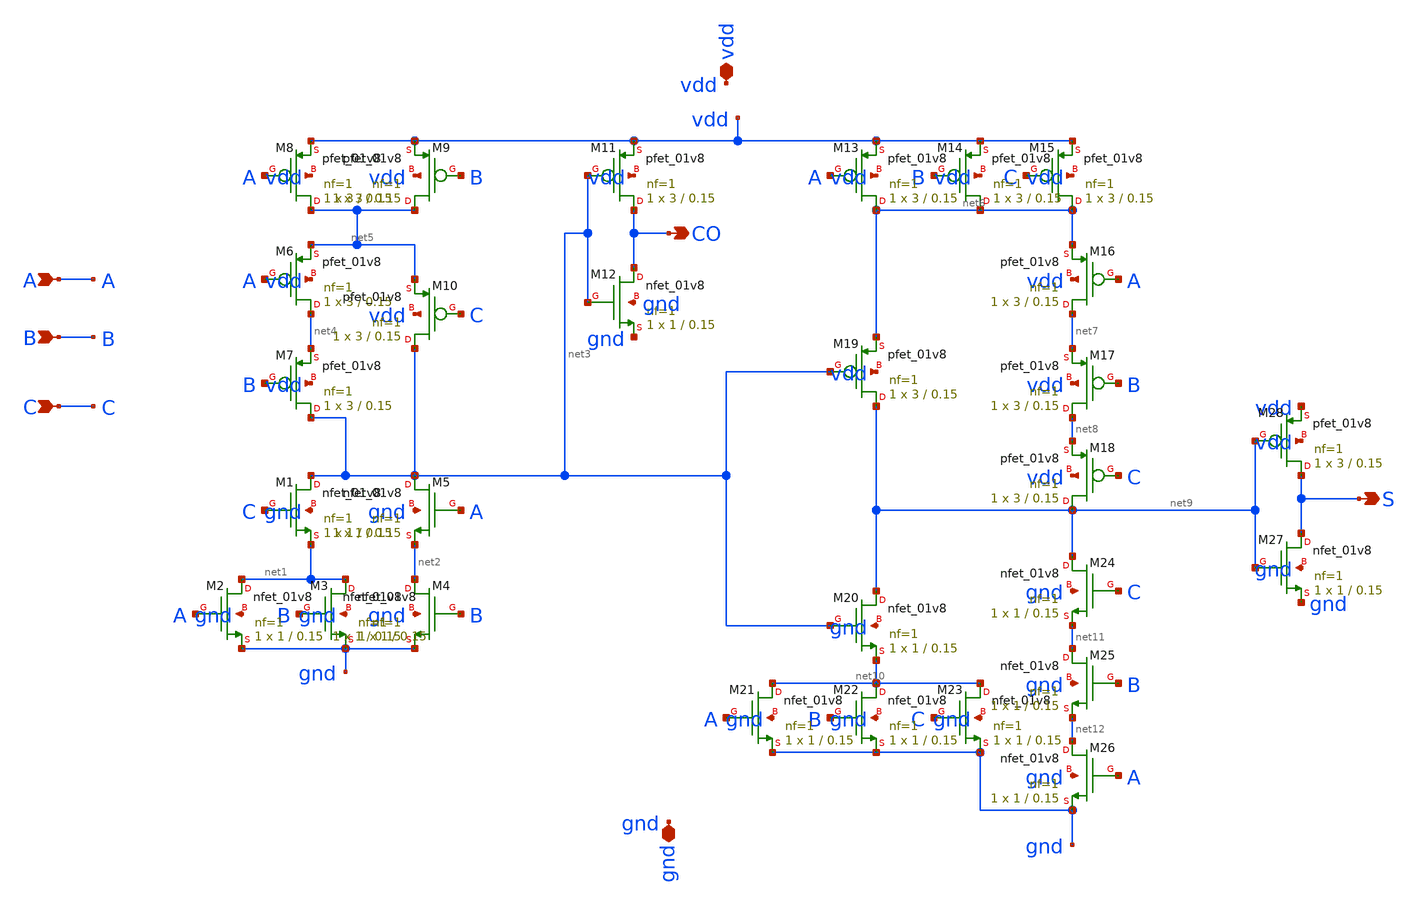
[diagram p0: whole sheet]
** sch_path: FullAdder1bit.sch
**.subckt FullAdder1bit CO S A B C vdd gnd
*.opin CO
*.opin S
*.ipin A
*.ipin B
*.ipin C
*.iopin vdd
*.iopin gnd
XM8 net5 A vdd vdd sky130_fd_pr__pfet_01v8 L=0.15 W=3 nf=1 ad='int((1 + 1)/2) * 3 / 1 * 0.29' as='int((1 + 2)/2) * 3 / 1 * 0.29'
+ pd='2*int((1 + 1)/2) * (3 / 1 + 0.29)' ps='2*int((1 + 2)/2) * (3 / 1 + 0.29)' nrd='0.29 / 3 ' nrs='0.29 / 3 '
+ sa=0 sb=0 sd=0 mult=1 m=1
XM12 CO net3 gnd gnd sky130_fd_pr__nfet_01v8 L=0.15 W=1 nf=1 ad='int((1 + 1)/2) * 1 / 1 * 0.29' as='int((1 + 2)/2) * 1 / 1 * 0.29'
+ pd='2*int((1 + 1)/2) * (1 / 1 + 0.29)' ps='2*int((1 + 2)/2) * (1 / 1 + 0.29)' nrd='0.29 / 1 ' nrs='0.29 / 1 '
+ sa=0 sb=0 sd=0 mult=1 m=1
XM1 net3 C net1 gnd sky130_fd_pr__nfet_01v8 L=0.15 W=1 nf=1 ad='int((1 + 1)/2) * 1 / 1 * 0.29' as='int((1 + 2)/2) * 1 / 1 * 0.29'
+ pd='2*int((1 + 1)/2) * (1 / 1 + 0.29)' ps='2*int((1 + 2)/2) * (1 / 1 + 0.29)' nrd='0.29 / 1 ' nrs='0.29 / 1 '
+ sa=0 sb=0 sd=0 mult=1 m=1
XM6 net4 A net5 vdd sky130_fd_pr__pfet_01v8 L=0.15 W=3 nf=1 ad='int((1 + 1)/2) * 3 / 1 * 0.29' as='int((1 + 2)/2) * 3 / 1 * 0.29'
+ pd='2*int((1 + 1)/2) * (3 / 1 + 0.29)' ps='2*int((1 + 2)/2) * (3 / 1 + 0.29)' nrd='0.29 / 3 ' nrs='0.29 / 3 '
+ sa=0 sb=0 sd=0 mult=1 m=1
XM7 net3 B net4 vdd sky130_fd_pr__pfet_01v8 L=0.15 W=3 nf=1 ad='int((1 + 1)/2) * 3 / 1 * 0.29' as='int((1 + 2)/2) * 3 / 1 * 0.29'
+ pd='2*int((1 + 1)/2) * (3 / 1 + 0.29)' ps='2*int((1 + 2)/2) * (3 / 1 + 0.29)' nrd='0.29 / 3 ' nrs='0.29 / 3 '
+ sa=0 sb=0 sd=0 mult=1 m=1
XM9 net5 B vdd vdd sky130_fd_pr__pfet_01v8 L=0.15 W=3 nf=1 ad='int((1 + 1)/2) * 3 / 1 * 0.29' as='int((1 + 2)/2) * 3 / 1 * 0.29'
+ pd='2*int((1 + 1)/2) * (3 / 1 + 0.29)' ps='2*int((1 + 2)/2) * (3 / 1 + 0.29)' nrd='0.29 / 3 ' nrs='0.29 / 3 '
+ sa=0 sb=0 sd=0 mult=1 m=1
XM10 net3 C net5 vdd sky130_fd_pr__pfet_01v8 L=0.15 W=3 nf=1 ad='int((1 + 1)/2) * 3 / 1 * 0.29' as='int((1 + 2)/2) * 3 / 1 * 0.29'
+ pd='2*int((1 + 1)/2) * (3 / 1 + 0.29)' ps='2*int((1 + 2)/2) * (3 / 1 + 0.29)' nrd='0.29 / 3 ' nrs='0.29 / 3 '
+ sa=0 sb=0 sd=0 mult=1 m=1
XM11 CO net3 vdd vdd sky130_fd_pr__pfet_01v8 L=0.15 W=3 nf=1 ad='int((1 + 1)/2) * 3 / 1 * 0.29' as='int((1 + 2)/2) * 3 / 1 * 0.29'
+ pd='2*int((1 + 1)/2) * (3 / 1 + 0.29)' ps='2*int((1 + 2)/2) * (3 / 1 + 0.29)' nrd='0.29 / 3 ' nrs='0.29 / 3 '
+ sa=0 sb=0 sd=0 mult=1 m=1
XM13 net6 A vdd vdd sky130_fd_pr__pfet_01v8 L=0.15 W=3 nf=1 ad='int((1 + 1)/2) * 3 / 1 * 0.29' as='int((1 + 2)/2) * 3 / 1 * 0.29'
+ pd='2*int((1 + 1)/2) * (3 / 1 + 0.29)' ps='2*int((1 + 2)/2) * (3 / 1 + 0.29)' nrd='0.29 / 3 ' nrs='0.29 / 3 '
+ sa=0 sb=0 sd=0 mult=1 m=1
XM14 net6 B vdd vdd sky130_fd_pr__pfet_01v8 L=0.15 W=3 nf=1 ad='int((1 + 1)/2) * 3 / 1 * 0.29' as='int((1 + 2)/2) * 3 / 1 * 0.29'
+ pd='2*int((1 + 1)/2) * (3 / 1 + 0.29)' ps='2*int((1 + 2)/2) * (3 / 1 + 0.29)' nrd='0.29 / 3 ' nrs='0.29 / 3 '
+ sa=0 sb=0 sd=0 mult=1 m=1
XM15 net6 C vdd vdd sky130_fd_pr__pfet_01v8 L=0.15 W=3 nf=1 ad='int((1 + 1)/2) * 3 / 1 * 0.29' as='int((1 + 2)/2) * 3 / 1 * 0.29'
+ pd='2*int((1 + 1)/2) * (3 / 1 + 0.29)' ps='2*int((1 + 2)/2) * (3 / 1 + 0.29)' nrd='0.29 / 3 ' nrs='0.29 / 3 '
+ sa=0 sb=0 sd=0 mult=1 m=1
XM16 net7 A net6 vdd sky130_fd_pr__pfet_01v8 L=0.15 W=3 nf=1 ad='int((1 + 1)/2) * 3 / 1 * 0.29' as='int((1 + 2)/2) * 3 / 1 * 0.29'
+ pd='2*int((1 + 1)/2) * (3 / 1 + 0.29)' ps='2*int((1 + 2)/2) * (3 / 1 + 0.29)' nrd='0.29 / 3 ' nrs='0.29 / 3 '
+ sa=0 sb=0 sd=0 mult=1 m=1
XM17 net8 B net7 vdd sky130_fd_pr__pfet_01v8 L=0.15 W=3 nf=1 ad='int((1 + 1)/2) * 3 / 1 * 0.29' as='int((1 + 2)/2) * 3 / 1 * 0.29'
+ pd='2*int((1 + 1)/2) * (3 / 1 + 0.29)' ps='2*int((1 + 2)/2) * (3 / 1 + 0.29)' nrd='0.29 / 3 ' nrs='0.29 / 3 '
+ sa=0 sb=0 sd=0 mult=1 m=1
XM18 net9 C net8 vdd sky130_fd_pr__pfet_01v8 L=0.15 W=3 nf=1 ad='int((1 + 1)/2) * 3 / 1 * 0.29' as='int((1 + 2)/2) * 3 / 1 * 0.29'
+ pd='2*int((1 + 1)/2) * (3 / 1 + 0.29)' ps='2*int((1 + 2)/2) * (3 / 1 + 0.29)' nrd='0.29 / 3 ' nrs='0.29 / 3 '
+ sa=0 sb=0 sd=0 mult=1 m=1
XM19 net9 net3 net6 vdd sky130_fd_pr__pfet_01v8 L=0.15 W=3 nf=1 ad='int((1 + 1)/2) * 3 / 1 * 0.29' as='int((1 + 2)/2) * 3 / 1 * 0.29'
+ pd='2*int((1 + 1)/2) * (3 / 1 + 0.29)' ps='2*int((1 + 2)/2) * (3 / 1 + 0.29)' nrd='0.29 / 3 ' nrs='0.29 / 3 '
+ sa=0 sb=0 sd=0 mult=1 m=1
XM2 net1 A gnd gnd sky130_fd_pr__nfet_01v8 L=0.15 W=1 nf=1 ad='int((1 + 1)/2) * 1 / 1 * 0.29' as='int((1 + 2)/2) * 1 / 1 * 0.29'
+ pd='2*int((1 + 1)/2) * (1 / 1 + 0.29)' ps='2*int((1 + 2)/2) * (1 / 1 + 0.29)' nrd='0.29 / 1 ' nrs='0.29 / 1 '
+ sa=0 sb=0 sd=0 mult=1 m=1
XM3 net1 B gnd gnd sky130_fd_pr__nfet_01v8 L=0.15 W=1 nf=1 ad='int((1 + 1)/2) * 1 / 1 * 0.29' as='int((1 + 2)/2) * 1 / 1 * 0.29'
+ pd='2*int((1 + 1)/2) * (1 / 1 + 0.29)' ps='2*int((1 + 2)/2) * (1 / 1 + 0.29)' nrd='0.29 / 1 ' nrs='0.29 / 1 '
+ sa=0 sb=0 sd=0 mult=1 m=1
XM4 net2 B gnd gnd sky130_fd_pr__nfet_01v8 L=0.15 W=1 nf=1 ad='int((1 + 1)/2) * 1 / 1 * 0.29' as='int((1 + 2)/2) * 1 / 1 * 0.29'
+ pd='2*int((1 + 1)/2) * (1 / 1 + 0.29)' ps='2*int((1 + 2)/2) * (1 / 1 + 0.29)' nrd='0.29 / 1 ' nrs='0.29 / 1 '
+ sa=0 sb=0 sd=0 mult=1 m=1
XM5 net3 A net2 gnd sky130_fd_pr__nfet_01v8 L=0.15 W=1 nf=1 ad='int((1 + 1)/2) * 1 / 1 * 0.29' as='int((1 + 2)/2) * 1 / 1 * 0.29'
+ pd='2*int((1 + 1)/2) * (1 / 1 + 0.29)' ps='2*int((1 + 2)/2) * (1 / 1 + 0.29)' nrd='0.29 / 1 ' nrs='0.29 / 1 '
+ sa=0 sb=0 sd=0 mult=1 m=1
XM20 net9 net3 net10 gnd sky130_fd_pr__nfet_01v8 L=0.15 W=1 nf=1 ad='int((1 + 1)/2) * 1 / 1 * 0.29' as='int((1 + 2)/2) * 1 / 1 * 0.29'
+ pd='2*int((1 + 1)/2) * (1 / 1 + 0.29)' ps='2*int((1 + 2)/2) * (1 / 1 + 0.29)' nrd='0.29 / 1 ' nrs='0.29 / 1 '
+ sa=0 sb=0 sd=0 mult=1 m=1
XM21 net10 A gnd gnd sky130_fd_pr__nfet_01v8 L=0.15 W=1 nf=1 ad='int((1 + 1)/2) * 1 / 1 * 0.29' as='int((1 + 2)/2) * 1 / 1 * 0.29'
+ pd='2*int((1 + 1)/2) * (1 / 1 + 0.29)' ps='2*int((1 + 2)/2) * (1 / 1 + 0.29)' nrd='0.29 / 1 ' nrs='0.29 / 1 '
+ sa=0 sb=0 sd=0 mult=1 m=1
XM22 net10 B gnd gnd sky130_fd_pr__nfet_01v8 L=0.15 W=1 nf=1 ad='int((1 + 1)/2) * 1 / 1 * 0.29' as='int((1 + 2)/2) * 1 / 1 * 0.29'
+ pd='2*int((1 + 1)/2) * (1 / 1 + 0.29)' ps='2*int((1 + 2)/2) * (1 / 1 + 0.29)' nrd='0.29 / 1 ' nrs='0.29 / 1 '
+ sa=0 sb=0 sd=0 mult=1 m=1
XM23 net10 C gnd gnd sky130_fd_pr__nfet_01v8 L=0.15 W=1 nf=1 ad='int((1 + 1)/2) * 1 / 1 * 0.29' as='int((1 + 2)/2) * 1 / 1 * 0.29'
+ pd='2*int((1 + 1)/2) * (1 / 1 + 0.29)' ps='2*int((1 + 2)/2) * (1 / 1 + 0.29)' nrd='0.29 / 1 ' nrs='0.29 / 1 '
+ sa=0 sb=0 sd=0 mult=1 m=1
XM24 net9 C net11 gnd sky130_fd_pr__nfet_01v8 L=0.15 W=1 nf=1 ad='int((1 + 1)/2) * 1 / 1 * 0.29' as='int((1 + 2)/2) * 1 / 1 * 0.29'
+ pd='2*int((1 + 1)/2) * (1 / 1 + 0.29)' ps='2*int((1 + 2)/2) * (1 / 1 + 0.29)' nrd='0.29 / 1 ' nrs='0.29 / 1 '
+ sa=0 sb=0 sd=0 mult=1 m=1
XM25 net11 B net12 gnd sky130_fd_pr__nfet_01v8 L=0.15 W=1 nf=1 ad='int((1 + 1)/2) * 1 / 1 * 0.29' as='int((1 + 2)/2) * 1 / 1 * 0.29'
+ pd='2*int((1 + 1)/2) * (1 / 1 + 0.29)' ps='2*int((1 + 2)/2) * (1 / 1 + 0.29)' nrd='0.29 / 1 ' nrs='0.29 / 1 '
+ sa=0 sb=0 sd=0 mult=1 m=1
XM26 net12 A gnd gnd sky130_fd_pr__nfet_01v8 L=0.15 W=1 nf=1 ad='int((1 + 1)/2) * 1 / 1 * 0.29' as='int((1 + 2)/2) * 1 / 1 * 0.29'
+ pd='2*int((1 + 1)/2) * (1 / 1 + 0.29)' ps='2*int((1 + 2)/2) * (1 / 1 + 0.29)' nrd='0.29 / 1 ' nrs='0.29 / 1 '
+ sa=0 sb=0 sd=0 mult=1 m=1
XM27 S net9 gnd gnd sky130_fd_pr__nfet_01v8 L=0.15 W=1 nf=1 ad='int((1 + 1)/2) * 1 / 1 * 0.29' as='int((1 + 2)/2) * 1 / 1 * 0.29'
+ pd='2*int((1 + 1)/2) * (1 / 1 + 0.29)' ps='2*int((1 + 2)/2) * (1 / 1 + 0.29)' nrd='0.29 / 1 ' nrs='0.29 / 1 '
+ sa=0 sb=0 sd=0 mult=1 m=1
XM28 S net9 vdd vdd sky130_fd_pr__pfet_01v8 L=0.15 W=3 nf=1 ad='int((1 + 1)/2) * 3 / 1 * 0.29' as='int((1 + 2)/2) * 3 / 1 * 0.29'
+ pd='2*int((1 + 1)/2) * (3 / 1 + 0.29)' ps='2*int((1 + 2)/2) * (3 / 1 + 0.29)' nrd='0.29 / 3 ' nrs='0.29 / 3 '
+ sa=0 sb=0 sd=0 mult=1 m=1
**.ends
.end
